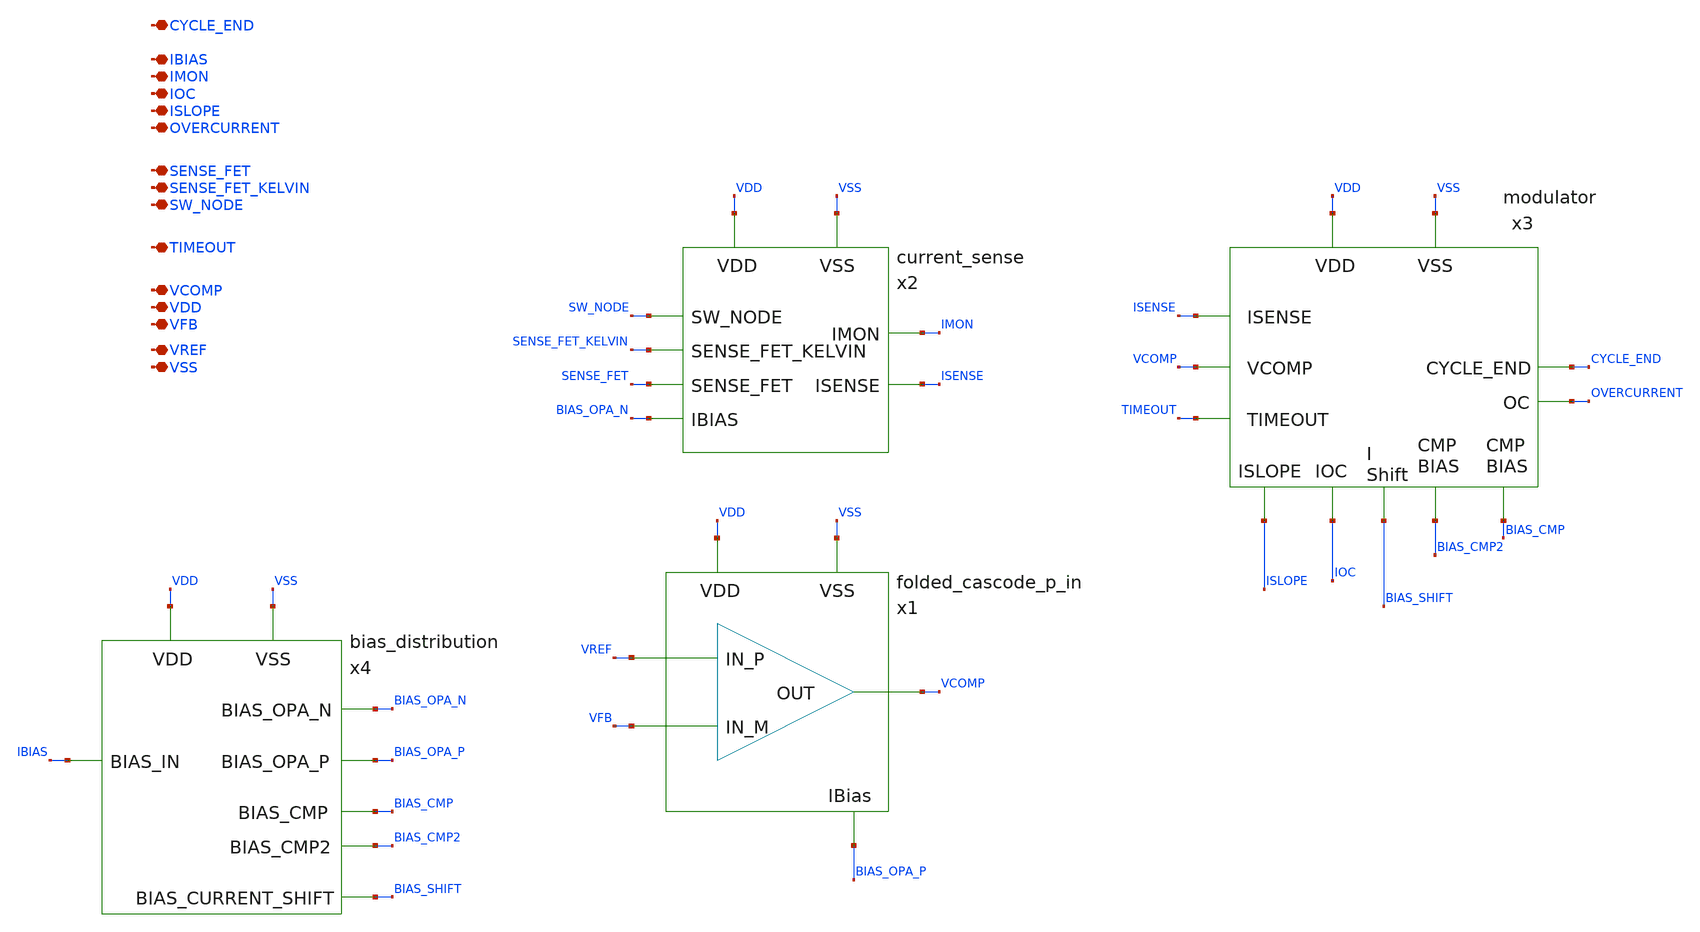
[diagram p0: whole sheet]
** sch_path: images/iic-osic-tools/addons/examples/Open-PMIC-tapeout/xschem/analog_subsystem.sch
**.subckt analog_subsystem CYCLE_END IBIAS IMON IOC ISLOPE OVERCURRENT SENSE_FET SENSE_FET_KELVIN
*+ SW_NODE TIMEOUT VCOMP VDD VFB VREF VSS
*.iopin CYCLE_END
*.iopin IBIAS
*.iopin IMON
*.iopin IOC
*.iopin ISLOPE
*.iopin OVERCURRENT
*.iopin SENSE_FET
*.iopin SENSE_FET_KELVIN
*.iopin SW_NODE
*.iopin TIMEOUT
*.iopin VCOMP
*.iopin VDD
*.iopin VFB
*.iopin VREF
*.iopin VSS
x3 VDD VSS BIAS_CMP ISLOPE ISENSE VCOMP TIMEOUT CYCLE_END BIAS_CMP2 IOC OVERCURRENT BIAS_SHIFT
+ modulator
x1 VREF VFB VCOMP VDD VSS BIAS_OPA_P folded_cascode_p_in
x2 VDD VSS SW_NODE SENSE_FET BIAS_OPA_N IMON ISENSE SENSE_FET_KELVIN current_sense
x4 VDD VSS IBIAS BIAS_OPA_N BIAS_OPA_P BIAS_CMP BIAS_CMP2 BIAS_SHIFT bias_distribution
**.ends
.end
